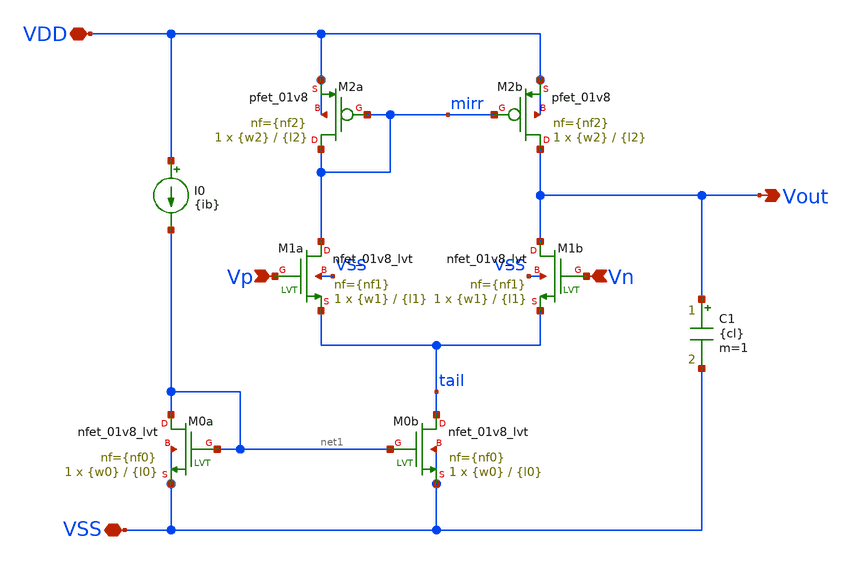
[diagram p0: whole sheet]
** sch_path: ota-5t-buf/xschem/ota-5t-buf.sch
**.subckt ota-5t-buf Vp Vn Vout VDD VSS
*.ipin Vp
*.ipin Vn
*.opin Vout
*.iopin VDD
*.iopin VSS
XM2b Vout mirr VDD VDD sky130_fd_pr__pfet_01v8 L={l2} W={w2} nf={nf2} ad='int((nf+1)/2) * W/nf * 0.29'
+ as='int((nf+2)/2) * W/nf * 0.29' pd='2*int((nf+1)/2) * (W/nf + 0.29)' ps='2*int((nf+2)/2) * (W/nf + 0.29)'
+ nrd='0.29 / W' nrs='0.29 / W' sa=0 sb=0 sd=0 mult=1 m=1
XM2a mirr mirr VDD VDD sky130_fd_pr__pfet_01v8 L={l2} W={w2} nf={nf2} ad='int((nf+1)/2) * W/nf * 0.29'
+ as='int((nf+2)/2) * W/nf * 0.29' pd='2*int((nf+1)/2) * (W/nf + 0.29)' ps='2*int((nf+2)/2) * (W/nf + 0.29)'
+ nrd='0.29 / W' nrs='0.29 / W' sa=0 sb=0 sd=0 mult=1 m=1
XM1a mirr Vp tail VSS sky130_fd_pr__nfet_01v8_lvt L={l1} W={w1} nf={nf1} ad='int((nf+1)/2) * W/nf * 0.29'
+ as='int((nf+2)/2) * W/nf * 0.29' pd='2*int((nf+1)/2) * (W/nf + 0.29)' ps='2*int((nf+2)/2) * (W/nf + 0.29)'
+ nrd='0.29 / W' nrs='0.29 / W' sa=0 sb=0 sd=0 mult=1 m=1
XM1b Vout Vn tail VSS sky130_fd_pr__nfet_01v8_lvt L={l1} W={w1} nf={nf1} ad='int((nf+1)/2) * W/nf * 0.29'
+ as='int((nf+2)/2) * W/nf * 0.29' pd='2*int((nf+1)/2) * (W/nf + 0.29)' ps='2*int((nf+2)/2) * (W/nf + 0.29)'
+ nrd='0.29 / W' nrs='0.29 / W' sa=0 sb=0 sd=0 mult=1 m=1
XM0b tail net1 VSS VSS sky130_fd_pr__nfet_01v8_lvt L={l0} W={w0} nf={nf0} ad='int((nf+1)/2) * W/nf * 0.29'
+ as='int((nf+2)/2) * W/nf * 0.29' pd='2*int((nf+1)/2) * (W/nf + 0.29)' ps='2*int((nf+2)/2) * (W/nf + 0.29)'
+ nrd='0.29 / W' nrs='0.29 / W' sa=0 sb=0 sd=0 mult=1 m=1
XM0a net1 net1 VSS VSS sky130_fd_pr__nfet_01v8_lvt L={l0} W={w0} nf={nf0} ad='int((nf+1)/2) * W/nf * 0.29'
+ as='int((nf+2)/2) * W/nf * 0.29' pd='2*int((nf+1)/2) * (W/nf + 0.29)' ps='2*int((nf+2)/2) * (W/nf + 0.29)'
+ nrd='0.29 / W' nrs='0.29 / W' sa=0 sb=0 sd=0 mult=1 m=1
I0 VDD net1 {ib}
C1 Vout VSS {cl} m=1
**.ends
.end
